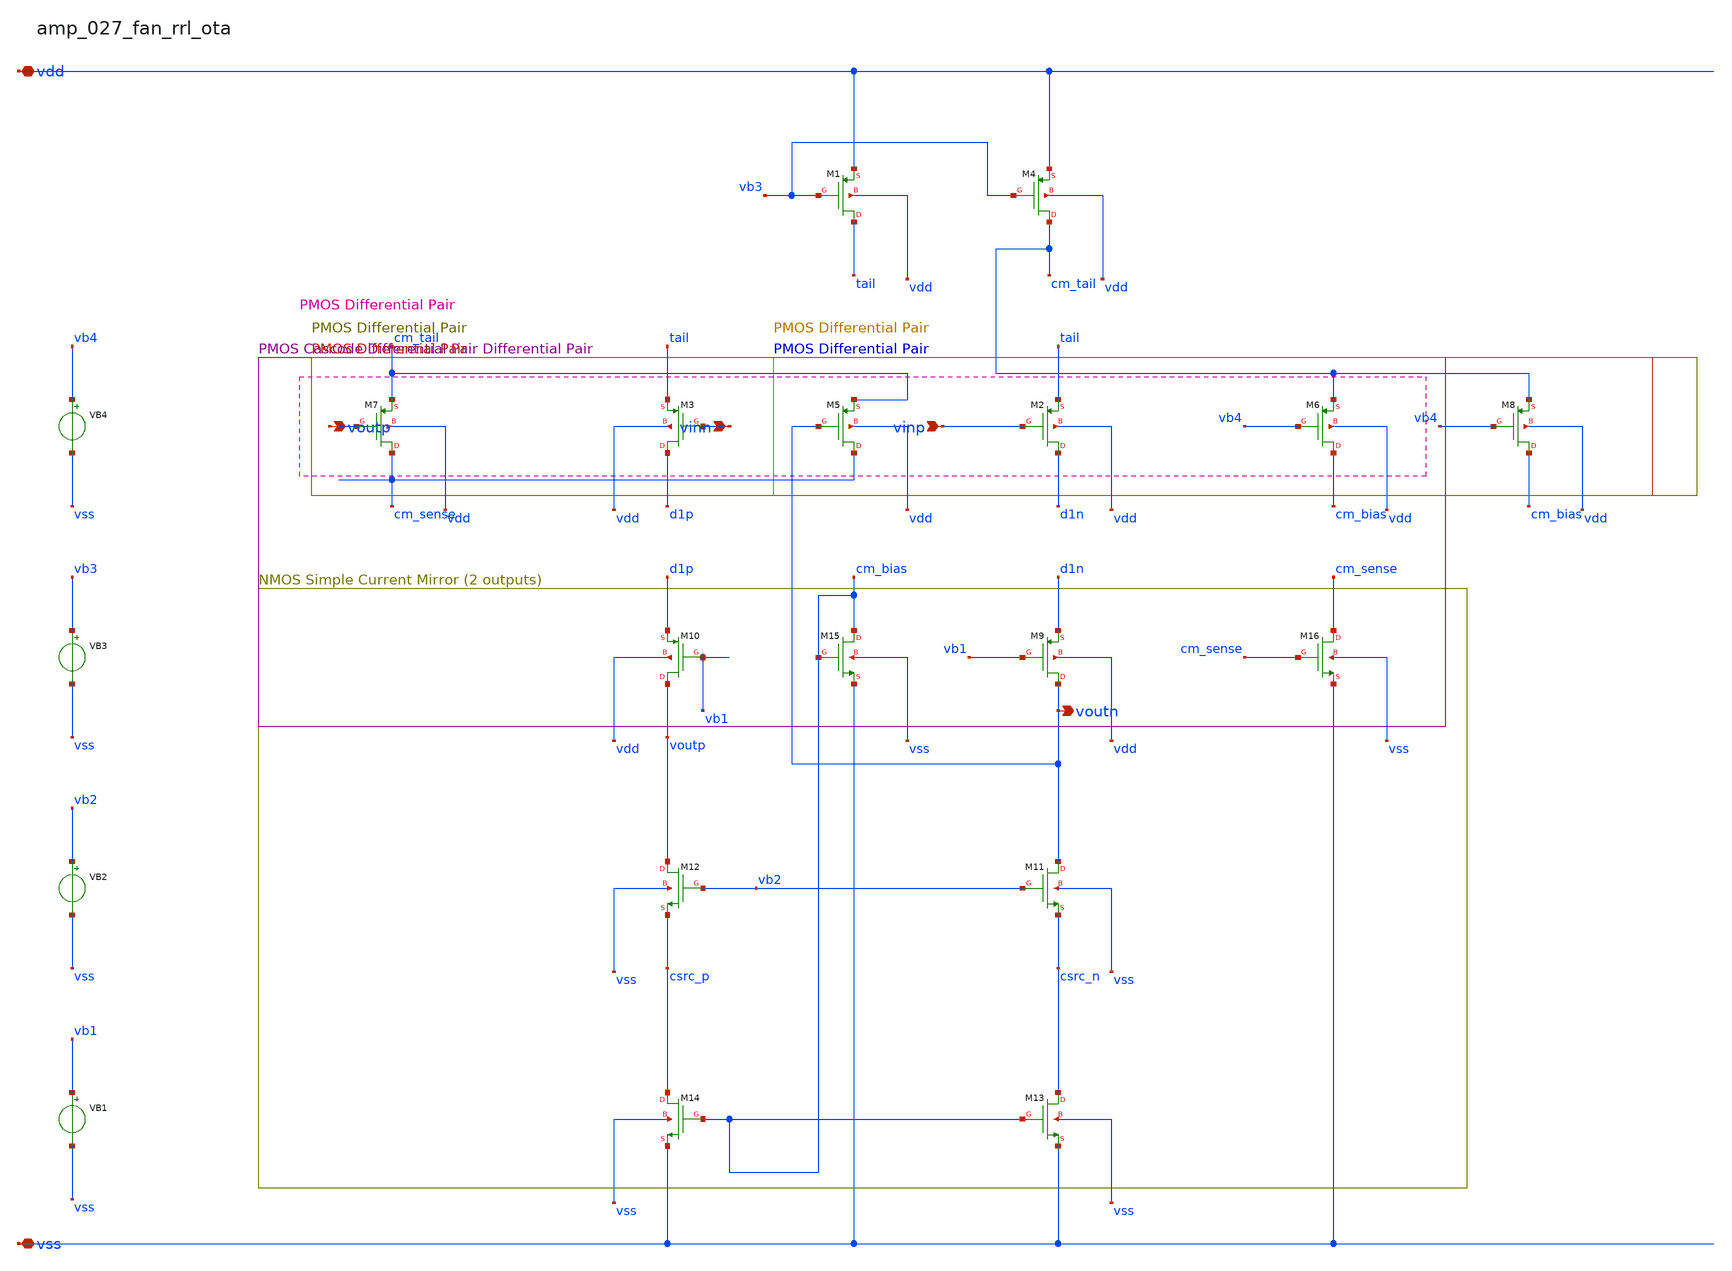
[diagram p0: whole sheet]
** sch_path: analog-db/raw/amp_027_fan_rrl_ota/amp_027_fan_rrl_ota_annotated.sch
**.subckt amp_027_fan_rrl_ota_annotated vinn vinp vdd vss voutp voutn
*.ipin vinn
*.ipin vinp
*.iopin vdd
*.iopin vss
*.opin voutp
*.opin voutn
VB1 vb1 vss dc {vb1}
VB2 vb2 vss dc {vb2}
VB3 vb3 vss dc {vb3}
VB4 vb4 vss dc {vb4}
XM1 tail vb3 vdd vdd sg13_lv_pmos w=x_dut_xm1_w l=x_dut_xm1_l ng=1 m=x_dut_xm1_m
XM10 voutp vb1 d1p vdd sg13_lv_pmos w=x_dut_xm10_w l=x_dut_xm10_l ng=1 m=x_dut_xm10_m
XM11 voutn vb2 csrc_n vss sg13_lv_nmos w=x_dut_xm11_w l=x_dut_xm11_l ng=1 m=x_dut_xm11_m
XM12 voutp vb2 csrc_p vss sg13_lv_nmos w=x_dut_xm12_w l=x_dut_xm12_l ng=1 m=x_dut_xm12_m
XM13 csrc_n cm_bias vss vss sg13_lv_nmos w=x_dut_xm13_w l=x_dut_xm13_l ng=1 m=x_dut_xm13_m
XM14 csrc_p cm_bias vss vss sg13_lv_nmos w=x_dut_xm14_w l=x_dut_xm14_l ng=1 m=x_dut_xm14_m
XM15 cm_bias cm_bias vss vss sg13_lv_nmos w=x_dut_xm15_w l=x_dut_xm15_l ng=1 m=x_dut_xm15_m
XM16 cm_sense cm_sense vss vss sg13_lv_nmos w=x_dut_xm16_w l=x_dut_xm16_l ng=1 m=x_dut_xm16_m
XM2 d1n vinp tail vdd sg13_lv_pmos w=x_dut_xm2_w l=x_dut_xm2_l ng=1 m=x_dut_xm2_m
XM3 d1p vinn tail vdd sg13_lv_pmos w=x_dut_xm3_w l=x_dut_xm3_l ng=1 m=x_dut_xm3_m
XM4 cm_tail vb3 vdd vdd sg13_lv_pmos w=x_dut_xm4_w l=x_dut_xm4_l ng=1 m=x_dut_xm4_m
XM5 cm_sense voutn cm_tail vdd sg13_lv_pmos w=x_dut_xm5_w l=x_dut_xm5_l ng=1 m=x_dut_xm5_m
XM6 cm_bias vb4 cm_tail vdd sg13_lv_pmos w=x_dut_xm6_w l=x_dut_xm6_l ng=1 m=x_dut_xm6_m
XM7 cm_sense voutp cm_tail vdd sg13_lv_pmos w=x_dut_xm7_w l=x_dut_xm7_l ng=1 m=x_dut_xm7_m
XM8 cm_bias vb4 cm_tail vdd sg13_lv_pmos w=x_dut_xm8_w l=x_dut_xm8_l ng=1 m=x_dut_xm8_m
XM9 voutn vb1 d1n vdd sg13_lv_pmos w=x_dut_xm9_w l=x_dut_xm9_l ng=1 m=x_dut_xm9_m
**.ends
.end
